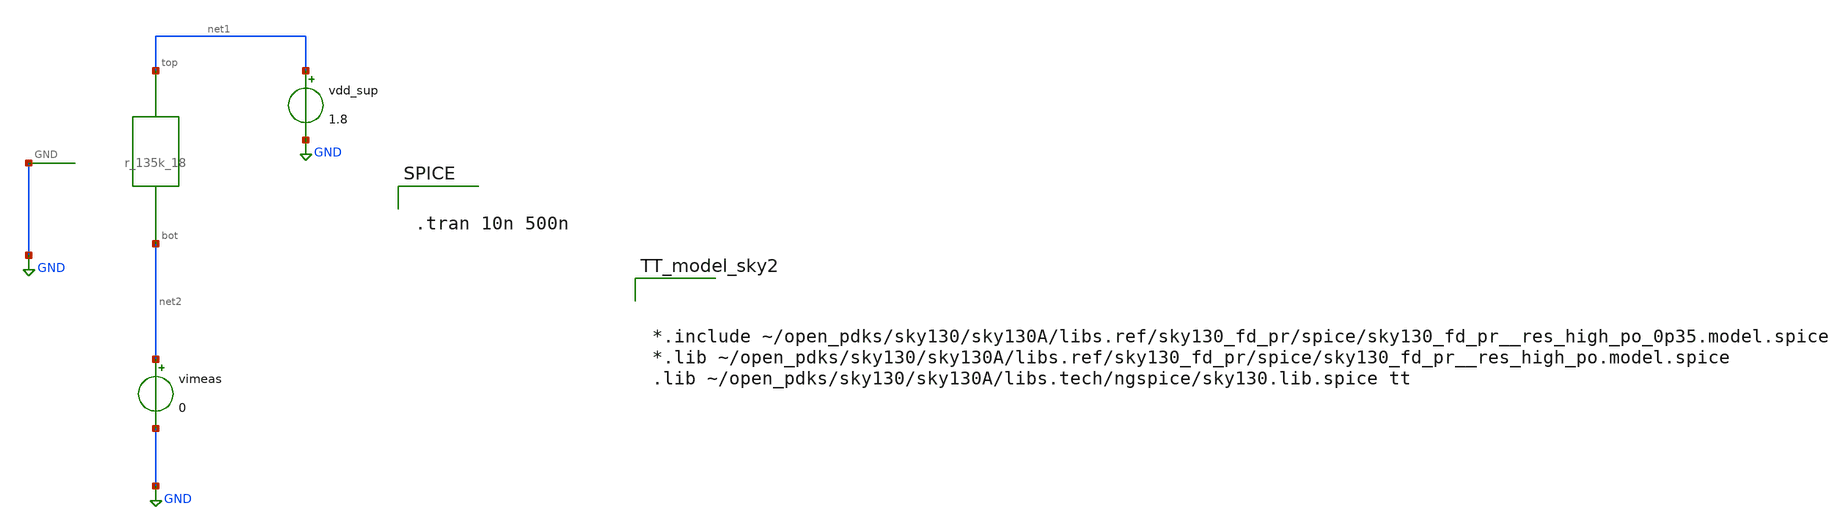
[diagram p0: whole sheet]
** sch_path: r135k_posttb.sch
**.subckt r135k_posttb
vdd_sup net1 GND 1.8
vimeas net2 GND 0
X1 net1 net2 GND r_135k_18
**** begin user architecture code


.tran 10n 500n




*.include ~/open_pdks/sky130/sky130A/libs.ref/sky130_fd_pr/spice/sky130_fd_pr__res_high_po_0p35.model.spice
*.lib ~/open_pdks/sky130/sky130A/libs.ref/sky130_fd_pr/spice/sky130_fd_pr__res_high_po.model.spice
.lib ~/open_pdks/sky130/sky130A/libs.tech/ngspice/sky130.lib.spice tt

**** end user architecture code
**.ends

* expanding   symbol:  /home/cegrahul/Downloads/r_135k_18.sym # of pins=3
** sym_path: r_135k_18.sym
** sch_path: r_135k_18.sch
.subckt r_135k_18 top bot GND
*.iopin bot
*.ipin GND
*.iopin top
XR2 net2 net1 GND sky130_fd_pr__res_high_po W=1 L=0.35 mult=1 m=1
XR3 net3 net2 GND sky130_fd_pr__res_high_po W=1 L=0.35 mult=1 m=1
XR4 net4 net3 GND sky130_fd_pr__res_high_po W=1 L=0.35 mult=1 m=1
XR5 net7 net4 GND sky130_fd_pr__res_high_po W=1 L=0.35 mult=1 m=1
XR6 net5 net7 GND sky130_fd_pr__res_high_po W=1 L=0.35 mult=1 m=1
XR7 net6 net5 GND sky130_fd_pr__res_high_po W=1 L=0.35 mult=1 m=1
XR8 bot net6 GND sky130_fd_pr__res_high_po W=1 L=0.35 mult=1 m=1
XR9 net6 net5 GND sky130_fd_pr__res_high_po W=1 L=0.35 mult=1 m=1
XR10 bot net6 GND sky130_fd_pr__res_high_po W=1 L=0.35 mult=1 m=1
XR11 bot net6 GND sky130_fd_pr__res_high_po W=1 L=0.35 mult=1 m=1
XR12 bot net6 GND sky130_fd_pr__res_high_po W=1 L=0.35 mult=1 m=1
XR13 net1 top GND sky130_fd_pr__res_high_po W=1 L=0.35 mult=1 m=1
.ends

.GLOBAL GND
.end
